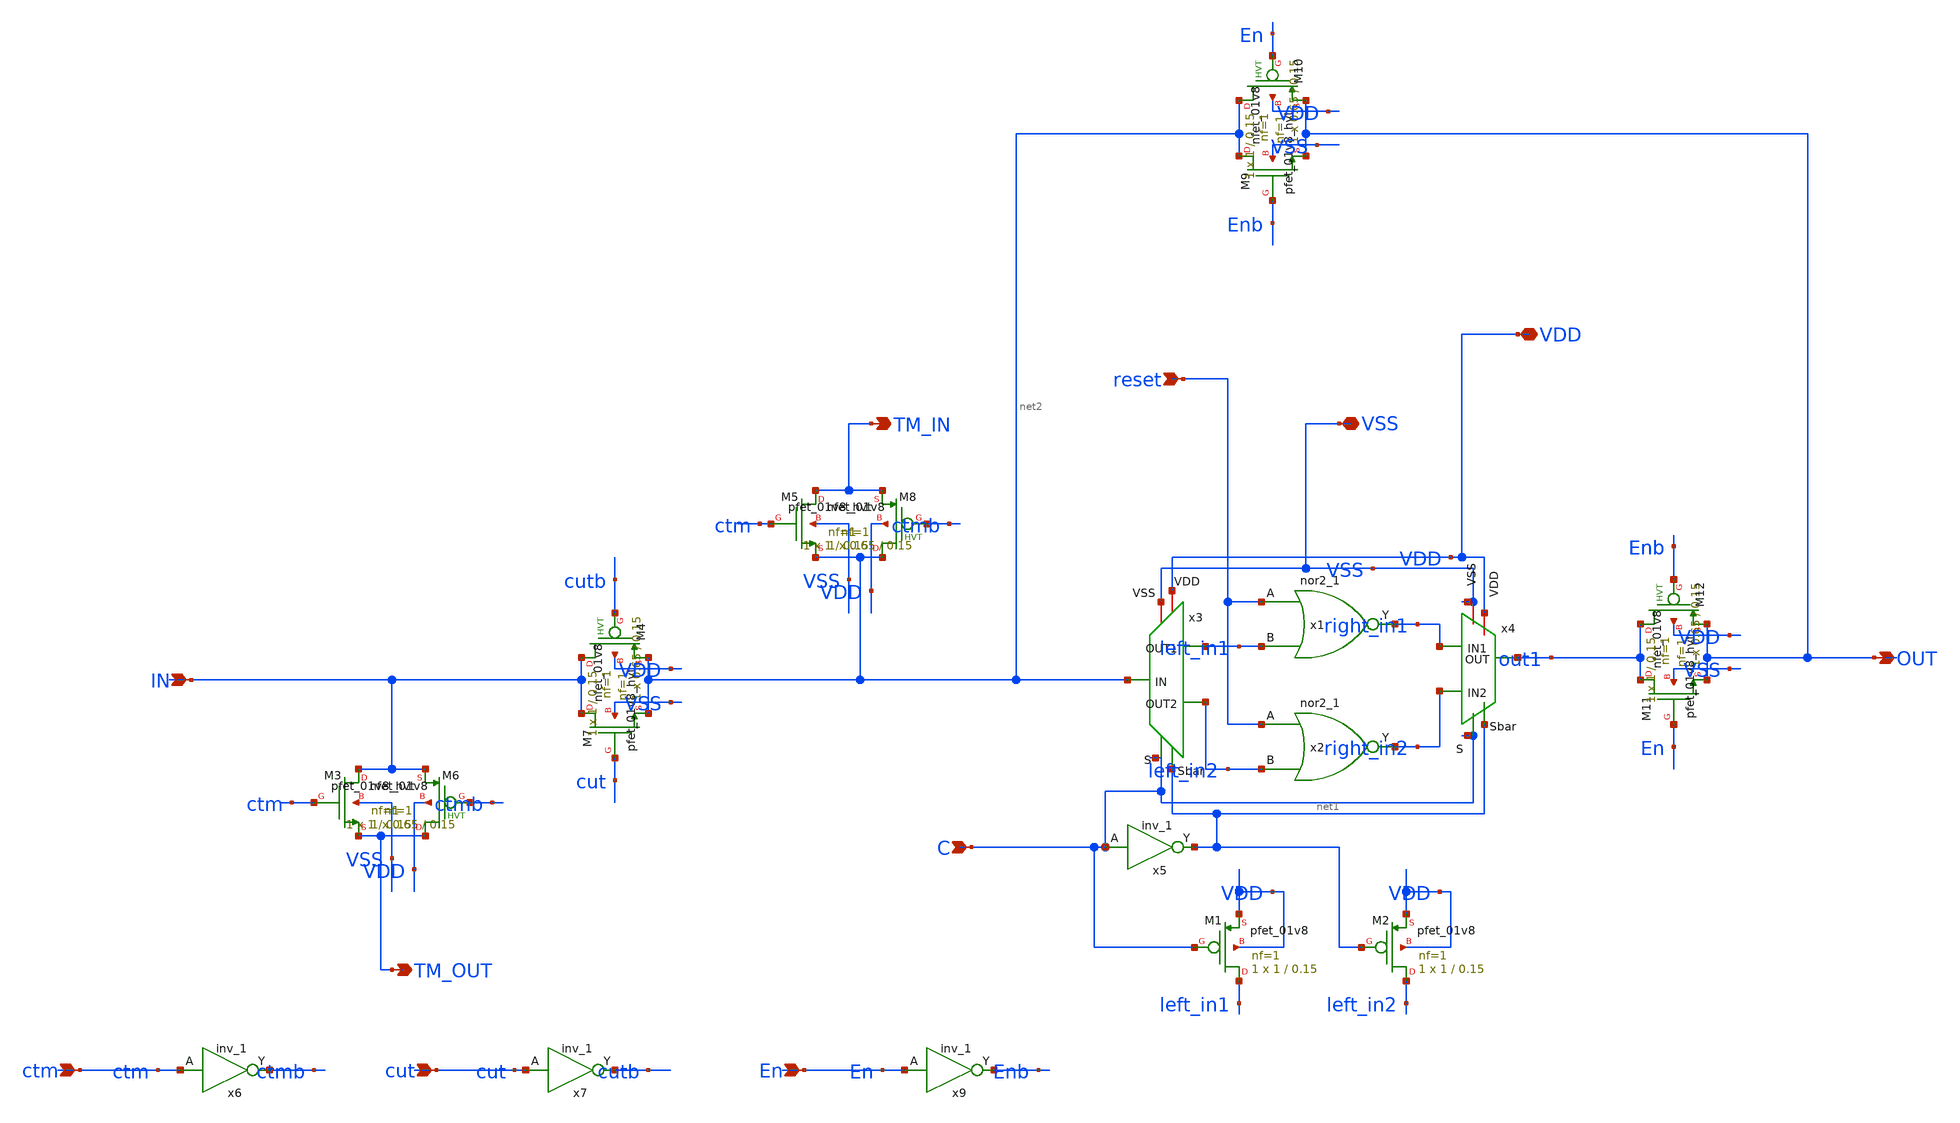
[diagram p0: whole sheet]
** sch_path: design/singlestage_floattm.sch
**.subckt singlestage_floattm IN reset OUT En C cut ctm VDD VSS TM_OUT TM_IN
*.ipin IN
*.ipin reset
*.opin OUT
*.ipin En
*.ipin C
*.ipin cut
*.ipin ctm
*.iopin VDD
*.iopin VSS
*.opin TM_OUT
*.opin TM_IN
x1 reset left_in1 GND GND VDD VDD right_in1 sky130_fd_sc_hd__nor2_1
x2 reset left_in2 GND GND VDD VDD right_in2 sky130_fd_sc_hd__nor2_1
x3 C VSS left_in1 VDD net2 net1 left_in2 demux2-1
x4 C VSS right_in1 VDD out1 net1 right_in2 mux2-1
x5 C GND GND VDD VDD net1 sky130_fd_sc_hd__inv_1
XM1 left_in1 C VDD VDD sky130_fd_pr__pfet_01v8 L=0.15 W=1 nf=1 ad='int((nf+1)/2) * W/nf * 0.29' as='int((nf+2)/2) * W/nf * 0.29'
+ pd='2*int((nf+1)/2) * (W/nf + 0.29)' ps='2*int((nf+2)/2) * (W/nf + 0.29)' nrd='0.29 / W' nrs='0.29 / W'
+ sa=0 sb=0 sd=0 mult=1 m=1
XM2 left_in2 net1 VDD VDD sky130_fd_pr__pfet_01v8 L=0.15 W=1 nf=1 ad='int((nf+1)/2) * W/nf * 0.29' as='int((nf+2)/2) * W/nf * 0.29'
+ pd='2*int((nf+1)/2) * (W/nf + 0.29)' ps='2*int((nf+2)/2) * (W/nf + 0.29)' nrd='0.29 / W' nrs='0.29 / W'
+ sa=0 sb=0 sd=0 mult=1 m=1
XM3 IN ctm TM_OUT VSS sky130_fd_pr__nfet_01v8 L=0.15 W=0.65 nf=1 ad='int((nf+1)/2) * W/nf * 0.29' as='int((nf+2)/2) * W/nf * 0.29'
+ pd='2*int((nf+1)/2) * (W/nf + 0.29)' ps='2*int((nf+2)/2) * (W/nf + 0.29)' nrd='0.29 / W' nrs='0.29 / W'
+ sa=0 sb=0 sd=0 mult=1 m=1
XM5 TM_IN ctm net2 VSS sky130_fd_pr__nfet_01v8 L=0.15 W=0.65 nf=1 ad='int((nf+1)/2) * W/nf * 0.29' as='int((nf+2)/2) * W/nf * 0.29'
+ pd='2*int((nf+1)/2) * (W/nf + 0.29)' ps='2*int((nf+2)/2) * (W/nf + 0.29)' nrd='0.29 / W' nrs='0.29 / W'
+ sa=0 sb=0 sd=0 mult=1 m=1
XM7 IN cut net2 VSS sky130_fd_pr__nfet_01v8 L=0.15 W=0.65 nf=1 ad='int((nf+1)/2) * W/nf * 0.29' as='int((nf+2)/2) * W/nf * 0.29'
+ pd='2*int((nf+1)/2) * (W/nf + 0.29)' ps='2*int((nf+2)/2) * (W/nf + 0.29)' nrd='0.29 / W' nrs='0.29 / W'
+ sa=0 sb=0 sd=0 mult=1 m=1
XM4 IN cutb net2 VDD sky130_fd_pr__pfet_01v8_hvt L=0.15 W=1 nf=1 ad='int((nf+1)/2) * W/nf * 0.29' as='int((nf+2)/2) * W/nf * 0.29'
+ pd='2*int((nf+1)/2) * (W/nf + 0.29)' ps='2*int((nf+2)/2) * (W/nf + 0.29)' nrd='0.29 / W' nrs='0.29 / W'
+ sa=0 sb=0 sd=0 mult=1 m=1
XM6 TM_OUT ctmb IN VDD sky130_fd_pr__pfet_01v8_hvt L=0.15 W=1 nf=1 ad='int((nf+1)/2) * W/nf * 0.29' as='int((nf+2)/2) * W/nf * 0.29'
+ pd='2*int((nf+1)/2) * (W/nf + 0.29)' ps='2*int((nf+2)/2) * (W/nf + 0.29)' nrd='0.29 / W' nrs='0.29 / W'
+ sa=0 sb=0 sd=0 mult=1 m=1
XM8 net2 ctmb TM_IN VDD sky130_fd_pr__pfet_01v8_hvt L=0.15 W=1 nf=1 ad='int((nf+1)/2) * W/nf * 0.29'
+ as='int((nf+2)/2) * W/nf * 0.29' pd='2*int((nf+1)/2) * (W/nf + 0.29)' ps='2*int((nf+2)/2) * (W/nf + 0.29)'
+ nrd='0.29 / W' nrs='0.29 / W' sa=0 sb=0 sd=0 mult=1 m=1
XM9 net2 Enb OUT VSS sky130_fd_pr__nfet_01v8 L=0.15 W=0.65 nf=1 ad='int((nf+1)/2) * W/nf * 0.29' as='int((nf+2)/2) * W/nf * 0.29'
+ pd='2*int((nf+1)/2) * (W/nf + 0.29)' ps='2*int((nf+2)/2) * (W/nf + 0.29)' nrd='0.29 / W' nrs='0.29 / W'
+ sa=0 sb=0 sd=0 mult=1 m=1
XM10 net2 En OUT VDD sky130_fd_pr__pfet_01v8_hvt L=0.15 W=1 nf=1 ad='int((nf+1)/2) * W/nf * 0.29' as='int((nf+2)/2) * W/nf * 0.29'
+ pd='2*int((nf+1)/2) * (W/nf + 0.29)' ps='2*int((nf+2)/2) * (W/nf + 0.29)' nrd='0.29 / W' nrs='0.29 / W'
+ sa=0 sb=0 sd=0 mult=1 m=1
XM11 out1 En OUT VSS sky130_fd_pr__nfet_01v8 L=0.15 W=0.65 nf=1 ad='int((nf+1)/2) * W/nf * 0.29' as='int((nf+2)/2) * W/nf * 0.29'
+ pd='2*int((nf+1)/2) * (W/nf + 0.29)' ps='2*int((nf+2)/2) * (W/nf + 0.29)' nrd='0.29 / W' nrs='0.29 / W'
+ sa=0 sb=0 sd=0 mult=1 m=1
XM12 out1 Enb OUT VDD sky130_fd_pr__pfet_01v8_hvt L=0.15 W=1 nf=1 ad='int((nf+1)/2) * W/nf * 0.29' as='int((nf+2)/2) * W/nf * 0.29'
+ pd='2*int((nf+1)/2) * (W/nf + 0.29)' ps='2*int((nf+2)/2) * (W/nf + 0.29)' nrd='0.29 / W' nrs='0.29 / W'
+ sa=0 sb=0 sd=0 mult=1 m=1
x6 ctm GND GND VDD VDD ctmb sky130_fd_sc_hd__inv_1
x7 cut GND GND VDD VDD cutb sky130_fd_sc_hd__inv_1
x9 En GND GND VDD VDD Enb sky130_fd_sc_hd__inv_1
**.ends

* expanding   symbol:  demux2-1.sym # of pins=7
** sym_path: xiaolin/demux2-1.sym
** sch_path: xiaolin/demux2-1.sch
.subckt demux2-1 S VSS OUT1 VDD IN Sbar OUT2
*.ipin Sbar
*.ipin S
*.iopin VSS
*.iopin VDD
*.opin OUT1
*.opin OUT2
*.ipin IN
XM2 IN S OUT1 VSS sky130_fd_pr__nfet_01v8 L=0.15 W=0.65 nf=1 ad='int((nf+1)/2) * W/nf * 0.29' as='int((nf+2)/2) * W/nf * 0.29'
+ pd='2*int((nf+1)/2) * (W/nf + 0.29)' ps='2*int((nf+2)/2) * (W/nf + 0.29)' nrd='0.29 / W' nrs='0.29 / W'
+ sa=0 sb=0 sd=0 mult=1 m=1
XM1 IN Sbar OUT2 VSS sky130_fd_pr__nfet_01v8 L=0.15 W=0.65 nf=1 ad='int((nf+1)/2) * W/nf * 0.29' as='int((nf+2)/2) * W/nf * 0.29'
+ pd='2*int((nf+1)/2) * (W/nf + 0.29)' ps='2*int((nf+2)/2) * (W/nf + 0.29)' nrd='0.29 / W' nrs='0.29 / W'
+ sa=0 sb=0 sd=0 mult=1 m=1
XM3 IN S OUT2 VDD sky130_fd_pr__pfet_01v8_hvt L=0.15 W=1 nf=1 ad='int((nf+1)/2) * W/nf * 0.29' as='int((nf+2)/2) * W/nf * 0.29'
+ pd='2*int((nf+1)/2) * (W/nf + 0.29)' ps='2*int((nf+2)/2) * (W/nf + 0.29)' nrd='0.29 / W' nrs='0.29 / W'
+ sa=0 sb=0 sd=0 mult=1 m=1
XM4 IN Sbar OUT1 VDD sky130_fd_pr__pfet_01v8_hvt L=0.15 W=1 nf=1 ad='int((nf+1)/2) * W/nf * 0.29' as='int((nf+2)/2) * W/nf * 0.29'
+ pd='2*int((nf+1)/2) * (W/nf + 0.29)' ps='2*int((nf+2)/2) * (W/nf + 0.29)' nrd='0.29 / W' nrs='0.29 / W'
+ sa=0 sb=0 sd=0 mult=1 m=1
XM5 IN S OUT2 VDD sky130_fd_pr__pfet_01v8_hvt L=0.15 W=1 nf=1 ad='int((nf+1)/2) * W/nf * 0.29' as='int((nf+2)/2) * W/nf * 0.29'
+ pd='2*int((nf+1)/2) * (W/nf + 0.29)' ps='2*int((nf+2)/2) * (W/nf + 0.29)' nrd='0.29 / W' nrs='0.29 / W'
+ sa=0 sb=0 sd=0 mult=1 m=1
.ends


* expanding   symbol:  mux2-1.sym # of pins=7
** sym_path: design/mux2-1.sym
** sch_path: design/mux2-1.sch
.subckt mux2-1 S VSS IN1 VDD OUT Sbar IN2
*.ipin IN1
*.ipin IN2
*.ipin Sbar
*.ipin S
*.opin OUT
*.iopin VSS
*.iopin VDD
XM2 IN1 S OUT VSS sky130_fd_pr__nfet_01v8 L=0.15 W=0.65 nf=1 ad='int((nf+1)/2) * W/nf * 0.29' as='int((nf+2)/2) * W/nf * 0.29'
+ pd='2*int((nf+1)/2) * (W/nf + 0.29)' ps='2*int((nf+2)/2) * (W/nf + 0.29)' nrd='0.29 / W' nrs='0.29 / W'
+ sa=0 sb=0 sd=0 mult=1 m=1
XM1 IN2 Sbar OUT VSS sky130_fd_pr__nfet_01v8 L=0.15 W=0.65 nf=1 ad='int((nf+1)/2) * W/nf * 0.29' as='int((nf+2)/2) * W/nf * 0.29'
+ pd='2*int((nf+1)/2) * (W/nf + 0.29)' ps='2*int((nf+2)/2) * (W/nf + 0.29)' nrd='0.29 / W' nrs='0.29 / W'
+ sa=0 sb=0 sd=0 mult=1 m=1
XM4 IN1 Sbar OUT VDD sky130_fd_pr__pfet_01v8_hvt L=0.15 W=1 nf=1 ad='int((nf+1)/2) * W/nf * 0.29' as='int((nf+2)/2) * W/nf * 0.29'
+ pd='2*int((nf+1)/2) * (W/nf + 0.29)' ps='2*int((nf+2)/2) * (W/nf + 0.29)' nrd='0.29 / W' nrs='0.29 / W'
+ sa=0 sb=0 sd=0 mult=1 m=1
XM5 IN2 S OUT VDD sky130_fd_pr__pfet_01v8_hvt L=0.15 W=1 nf=1 ad='int((nf+1)/2) * W/nf * 0.29' as='int((nf+2)/2) * W/nf * 0.29'
+ pd='2*int((nf+1)/2) * (W/nf + 0.29)' ps='2*int((nf+2)/2) * (W/nf + 0.29)' nrd='0.29 / W' nrs='0.29 / W'
+ sa=0 sb=0 sd=0 mult=1 m=1
.ends

.end
